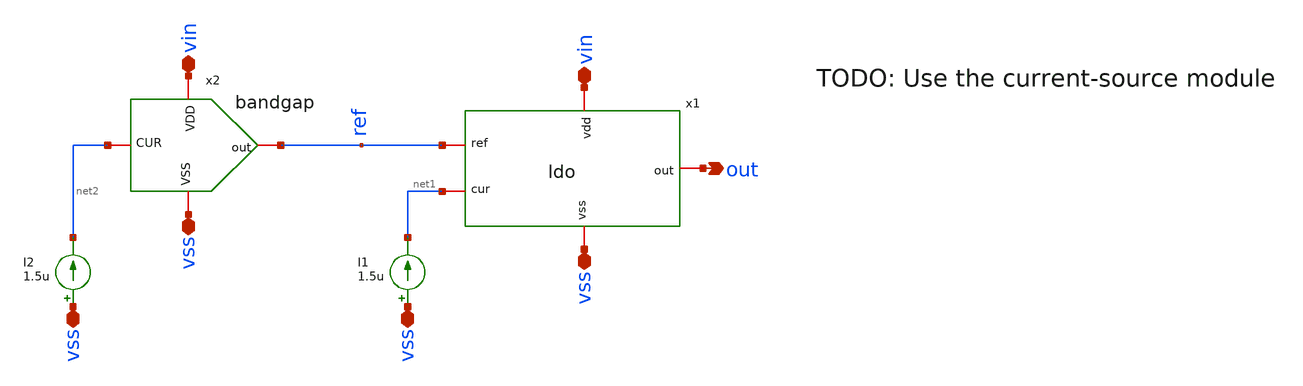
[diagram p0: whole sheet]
** sch_path: LDO/xschem/ldo-top/ldo-top.sch

.include $env(PDK_ROOT)/$env(PDK)/libs.tech/ngspice/design.ngspice

.lib $env(PDK_ROOT)/$env(PDK)/libs.tech/ngspice/sm141064.ngspice typical
.lib $env(PDK_ROOT)/$env(PDK)/libs.tech/ngspice/sm141064.ngspice mimcap_statistical
.lib $env(PDK_ROOT)/$env(PDK)/libs.tech/ngspice/sm141064.ngspice cap_mim
.lib $env(PDK_ROOT)/$env(PDK)/libs.tech/ngspice/sm141064.ngspice res_typical
.lib $env(PDK_ROOT)/$env(PDK)/libs.tech/ngspice/sm141064.ngspice bjt_typical
.lib $env(PDK_ROOT)/$env(PDK)/libs.tech/ngspice/sm141064.ngspice moscap_typical


**.subckt ldo-top out vin vss vin vss vss vss
*.opin out
*.iopin vin
*.iopin vss
*.iopin vin
*.iopin vss
*.iopin vss
*.iopin vss
I1 vss net1 1.5u
x1 vin ref net1 out vss ldo
x2 vin ref net2 vss bandgap
I2 vss net2 1.5u
**.ends
.end
